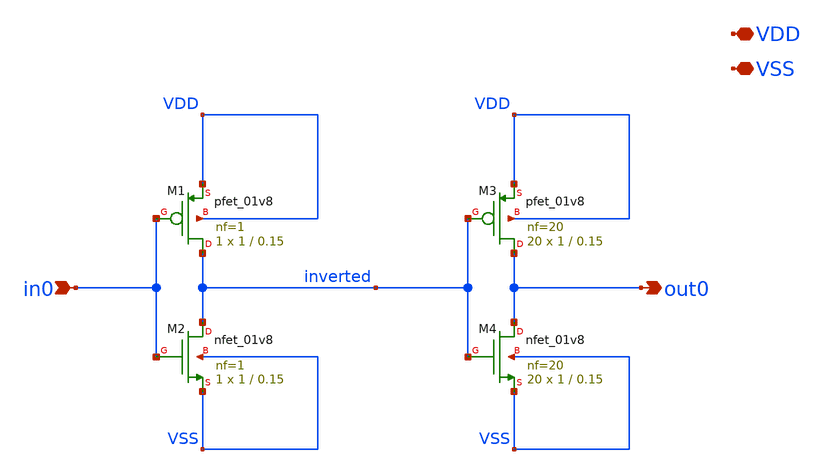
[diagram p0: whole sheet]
** sch_path: xschem/konstt-new-inv.sch
**.subckt konstt-new-inv VDD VSS in0 out0
*.iopin VDD
*.iopin VSS
*.ipin in0
*.opin out0
XM1 inverted in0 VDD VDD sky130_fd_pr__pfet_01v8 L=0.15 W=1 nf=1 ad='int((nf+1)/2) * W/nf * 0.29' as='int((nf+2)/2) * W/nf * 0.29'
+ pd='2*int((nf+1)/2) * (W/nf + 0.29)' ps='2*int((nf+2)/2) * (W/nf + 0.29)' nrd='0.29 / W' nrs='0.29 / W'
+ sa=0 sb=0 sd=0 mult=1 m=1
XM2 inverted in0 VSS VSS sky130_fd_pr__nfet_01v8 L=0.15 W=1 nf=1 ad='int((nf+1)/2) * W/nf * 0.29' as='int((nf+2)/2) * W/nf * 0.29'
+ pd='2*int((nf+1)/2) * (W/nf + 0.29)' ps='2*int((nf+2)/2) * (W/nf + 0.29)' nrd='0.29 / W' nrs='0.29 / W'
+ sa=0 sb=0 sd=0 mult=1 m=1
XM3 out0 inverted VDD VDD sky130_fd_pr__pfet_01v8 L=0.15 W=1 nf=20 ad='int((nf+1)/2) * W/nf * 0.29' as='int((nf+2)/2) * W/nf * 0.29'
+ pd='2*int((nf+1)/2) * (W/nf + 0.29)' ps='2*int((nf+2)/2) * (W/nf + 0.29)' nrd='0.29 / W' nrs='0.29 / W'
+ sa=0 sb=0 sd=0 mult=20 m=20
XM4 out0 inverted VSS VSS sky130_fd_pr__nfet_01v8 L=0.15 W=1 nf=20 ad='int((nf+1)/2) * W/nf * 0.29' as='int((nf+2)/2) * W/nf * 0.29'
+ pd='2*int((nf+1)/2) * (W/nf + 0.29)' ps='2*int((nf+2)/2) * (W/nf + 0.29)' nrd='0.29 / W' nrs='0.29 / W'
+ sa=0 sb=0 sd=0 mult=20 m=20
**.ends
.end
